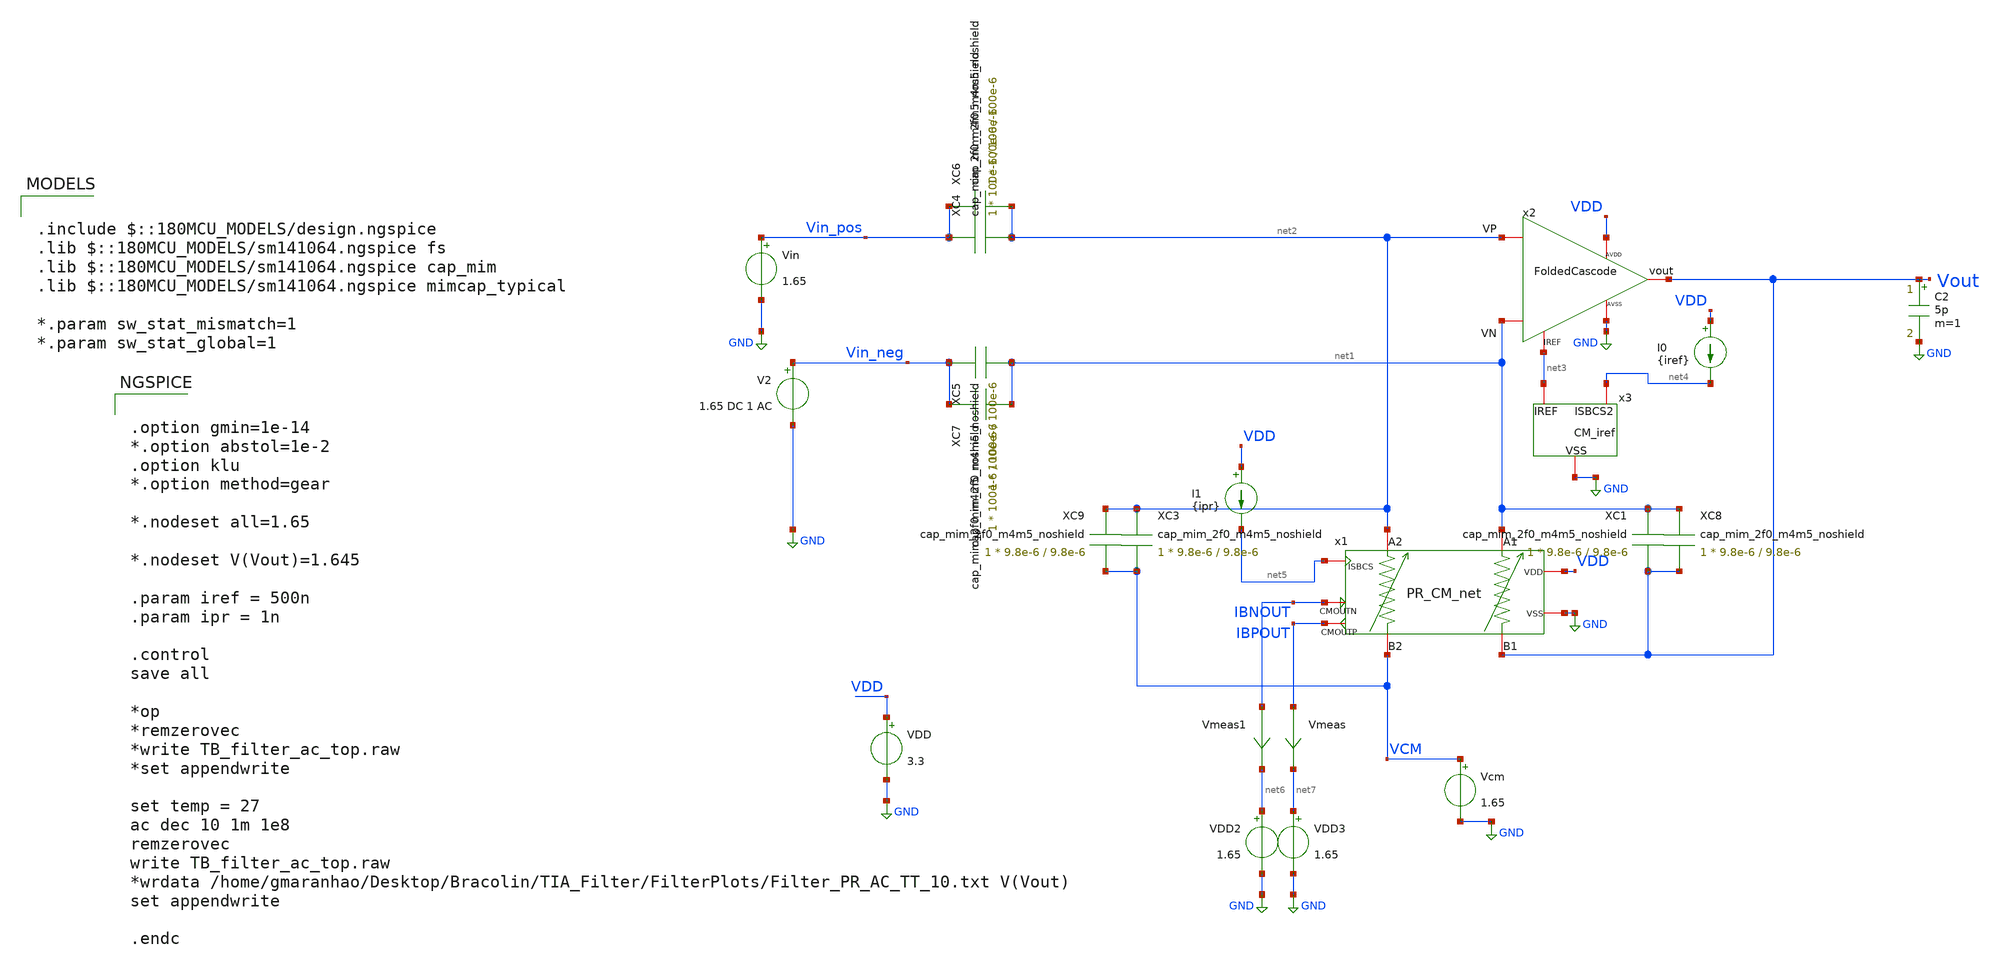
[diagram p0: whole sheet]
** sch_path: TIA_Filter/TB_filter_ac_top.sch
**.subckt TB_filter_ac_top
C2 Vout GND 5p m=1
V2 Vin_neg GND 1.65 DC 1 AC
x1 net5 net1 net2 VCM Vout IBNOUT IBPOUT VDD GND PR_CM_net
XC1 net1 Vout cap_mim_2f0_m4m5_noshield c_width=9.8e-6 c_length=9.8e-6 m=1
x2 net2 net1 Vout net3 VDD GND FoldedCascode
XC3 net2 VCM cap_mim_2f0_m4m5_noshield c_width=9.8e-6 c_length=9.8e-6 m=1
XC4 Vin_pos net2 cap_mim_2f0_m4m5_noshield c_width=100e-6 c_length=100e-6 m=1
XC5 Vin_neg net1 cap_mim_2f0_m4m5_noshield c_width=100e-6 c_length=100e-6 m=1
x3 net4 net3 GND CM_iref
I0 VDD net4 {iref}
I1 VDD net5 {ipr}
Vmeas IBPOUT net7 0
.save i(vmeas)
Vmeas1 IBNOUT net6 0
.save i(vmeas1)
Vcm VCM GND 1.65
VDD2 net6 GND 1.65
VDD3 net7 GND 1.65
VDD VDD GND 3.3
XC6 Vin_pos net2 cap_mim_2f0_m4m5_noshield c_width=100e-6 c_length=100e-6 m=1
XC7 Vin_neg net1 cap_mim_2f0_m4m5_noshield c_width=100e-6 c_length=100e-6 m=1
XC8 net1 Vout cap_mim_2f0_m4m5_noshield c_width=9.8e-6 c_length=9.8e-6 m=1
XC9 net2 VCM cap_mim_2f0_m4m5_noshield c_width=9.8e-6 c_length=9.8e-6 m=1
Vin Vin_pos GND 1.65
**** begin user architecture code

.include $::180MCU_MODELS/design.ngspice
.lib $::180MCU_MODELS/sm141064.ngspice fs
.lib $::180MCU_MODELS/sm141064.ngspice cap_mim
.lib $::180MCU_MODELS/sm141064.ngspice mimcap_typical

*.param sw_stat_mismatch=1
*.param sw_stat_global=1



.option gmin=1e-14
*.option abstol=1e-2
.option klu
*.option method=gear

*.nodeset all=1.65

*.nodeset V(Vout)=1.645

.param iref = 500n
.param ipr = 1n

.control
save all

*op
*remzerovec
*write TB_filter_ac_top.raw
*set appendwrite

set temp = 27
ac dec 10 1m 1e8
remzerovec
write TB_filter_ac_top.raw
*wrdata /home/gmaranhao/Desktop/Bracolin/TIA_Filter/FilterPlots/Filter_PR_AC_TT_10.txt V(Vout)
set appendwrite

.endc


**** end user architecture code
**.ends
.GLOBAL GND
.end
